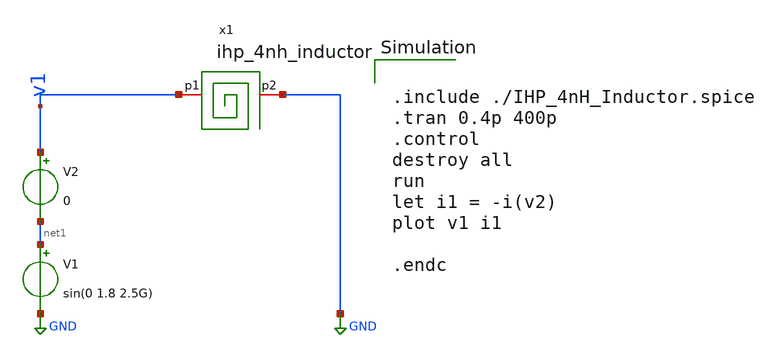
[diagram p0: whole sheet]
** sch_path: xschem/lc-vco/inductor/tb-tran.sch
**.subckt tb-tran
V1 net1 GND sin(0 1.8 2.5G)
V2 v1 net1 0
x1 v1 GND ihp_4nh_inductor
**** begin user architecture code


.include ./IHP_4nH_Inductor.spice
.tran 0.4p 400p
.control
destroy all
run
let i1 = -i(v2)
plot v1 i1

.endc

**** end user architecture code
**.ends
.GLOBAL GND
.end
